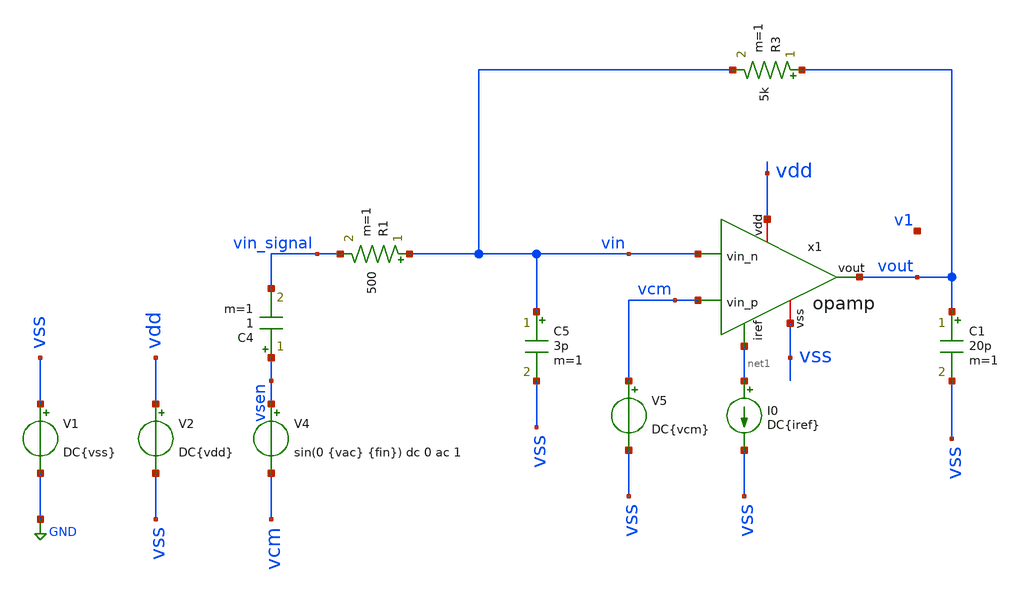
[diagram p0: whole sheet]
** sch_path: opamp/fftb_opamp_closeloop.sch
**.subckt fftb_opamp_closeloop
V1 vss GND DC{vss}
V2 vdd vss DC{vdd}
V4 vsen vcm sin(0 {vac} {fin}) dc 0 ac 1
C4 vsen vin_signal 1 m=1
I0 net1 vss DC{iref}
R1 vin vin_signal 500 m=1
R3 vout vin 5k m=1
C5 vin vss 3p m=1
C1 vout vss 20p m=1
V5 vcm vss DC{vcm}
x1 vdd net1 vin vcm vout vss v1 opamp
**** begin user architecture code




* Circuit Parameters
.param iref = 105u
.param vdd  = 1.98
.param vss  = 0.0
.param vcm  = 0.88
.param vac  = 60m
.param fin  = 9.765625e5
.options TEMP = 0

* FFT Parameters
.param Ts_FFT     = 1e-9
.csparam Ts_FFT   = {Ts_FFT}
.param fin_approx = 1e6
.param NFFT       = 4096
.csparam NFFT     = {NFFT}
.param vac_fin    = 'floor(fin_approx*Ts_FFT*NFFT)/Ts_FFT/NFFT'
.csparam Ti_FFT   = 3u
.csparam vac_fin  = {vac_fin}

* Include Models
*.lib ~/skywater/skywater-pdk/libraries/sky130_fd_pr_ngspice/latest/models/corners/sky130.lib TT
*.lib /foss/pdks/sky130A/libs.tech/ngspice/sky130.lib.spice.tt.red tt
*.lib ~/skywater/skywater-pdk/libraries/sky130_fd_pr_ngspice/latest/models/corners/sky130.lib TT
.lib /foss/pdks/sky130A/libs.tech/ngspice/sky130.lib.spice ff
*.lib /foss/pdks/sky130A/libs.tech/ngspice/sky130.lib.spice.tt.red tt
* OP Parameters & Singals to save
.save all  @M.X1.XM1.msky130_fd_pr__pfet_01v8_lvt[id] @M.X1.XM1.msky130_fd_pr__pfet_01v8_lvt[vth] @M.X1.XM1.msky130_fd_pr__pfet_01v8_lvt[vgs] @M.X1.XM1.msky130_fd_pr__pfet_01v8_lvt[vds] @M.X1.XM1.msky130_fd_pr__pfet_01v8_lvt[vdsat] @M.X1.XM1.msky130_fd_pr__pfet_01v8_lvt[gm] @M.X1.XM1.msky130_fd_pr__pfet_01v8_lvt[gds]  @M.X1.XM2.msky130_fd_pr__pfet_01v8_lvt[id] @M.X1.XM2.msky130_fd_pr__pfet_01v8_lvt[vth] @M.X1.XM2.msky130_fd_pr__pfet_01v8_lvt[vgs] @M.X1.XM2.msky130_fd_pr__pfet_01v8_lvt[vds] @M.X1.XM2.msky130_fd_pr__pfet_01v8_lvt[vdsat] @M.X1.XM2.msky130_fd_pr__pfet_01v8_lvt[gm] @M.X1.XM2.msky130_fd_pr__pfet_01v8_lvt[gds]  @M.X1.XM3.msky130_fd_pr__nfet_01v8[id] @M.X1.XM3.msky130_fd_pr__nfet_01v8[vth] @M.X1.XM3.msky130_fd_pr__nfet_01v8[vgs] @M.X1.XM3.msky130_fd_pr__nfet_01v8[vds] @M.X1.XM3.msky130_fd_pr__nfet_01v8[vdsat] @M.X1.XM3.msky130_fd_pr__nfet_01v8[gm] @M.X1.XM3.msky130_fd_pr__nfet_01v8[gds]  @M.X1.XM4.msky130_fd_pr__nfet_01v8[id] @M.X1.XM4.msky130_fd_pr__nfet_01v8[vth] @M.X1.XM4.msky130_fd_pr__nfet_01v8[vgs] @M.X1.XM4.msky130_fd_pr__nfet_01v8[vds] @M.X1.XM4.msky130_fd_pr__nfet_01v8[vdsat] @M.X1.XM4.msky130_fd_pr__nfet_01v8[gm] @M.X1.XM4.msky130_fd_pr__nfet_01v8[gds]  @M.X1.XM5.msky130_fd_pr__pfet_01v8[id] @M.X1.XM5.msky130_fd_pr__pfet_01v8[vth] @M.X1.XM5.msky130_fd_pr__pfet_01v8[vgs] @M.X1.XM5.msky130_fd_pr__pfet_01v8[vds] @M.X1.XM5.msky130_fd_pr__pfet_01v8[vdsat] @M.X1.XM5.msky130_fd_pr__pfet_01v8[gm] @M.X1.XM5.msky130_fd_pr__pfet_01v8[gds]  @M.X1.XM6.msky130_fd_pr__nfet_01v8[id] @M.X1.XM6.msky130_fd_pr__nfet_01v8[vth] @M.X1.XM6.msky130_fd_pr__nfet_01v8[vgs] @M.X1.XM6.msky130_fd_pr__nfet_01v8[vds] @M.X1.XM6.msky130_fd_pr__nfet_01v8[vdsat] @M.X1.XM6.msky130_fd_pr__nfet_01v8[gm] @M.X1.XM6.msky130_fd_pr__nfet_01v8[gds]  @M.X1.XM7.msky130_fd_pr__pfet_01v8[id] @M.X1.XM7.msky130_fd_pr__pfet_01v8[vth] @M.X1.XM7.msky130_fd_pr__pfet_01v8[vgs] @M.X1.XM7.msky130_fd_pr__pfet_01v8[vds] @M.X1.XM7.msky130_fd_pr__pfet_01v8[vdsat] @M.X1.XM7.msky130_fd_pr__pfet_01v8[gm] @M.X1.XM7.msky130_fd_pr__pfet_01v8[gds]  @M.X1.XM8.msky130_fd_pr__pfet_01v8[id] @M.X1.XM8.msky130_fd_pr__pfet_01v8[vth] @M.X1.XM8.msky130_fd_pr__pfet_01v8[vgs] @M.X1.XM8.msky130_fd_pr__pfet_01v8[vds] @M.X1.XM8.msky130_fd_pr__pfet_01v8[vdsat] @M.X1.XM8.msky130_fd_pr__pfet_01v8[gm] @M.X1.XM8.msky130_fd_pr__pfet_01v8[gds]  @M.X1.XM9.msky130_fd_pr__nfet_01v8[id] @M.X1.XM9.msky130_fd_pr__nfet_01v8[vth] @M.X1.XM9.msky130_fd_pr__nfet_01v8[vgs] @M.X1.XM9.msky130_fd_pr__nfet_01v8[vds] @M.X1.XM9.msky130_fd_pr__nfet_01v8[vdsat] @M.X1.XM9.msky130_fd_pr__nfet_01v8[gm] @M.X1.XM9.msky130_fd_pr__nfet_01v8[gds]

*Simulation
.control
  set color0 = white

  ac dec 100 1k 10G
  setplot ac1
  meas ac GBW when vdb(vout)=0
  meas ac DCG find vdb(vout) at=1k
  meas ac PM find vp(vout) when vdb(vout)=0
  print PM*180/PI
  plot vdb(vout) {vp(vout)*180/PI} vdb(v1) {vp(v1)*180/PI}

  reset
  tran 0.01u 11u
  setplot tran1
  plot v(vsen) v(vout)

  *reset
  *set sqrnoise
  *noise v(vout) V4 dec 100 1k 10G 1
  *let onoise_total_integrado = maximum(sqrt(integ(onoise_spectrum)))
  *print onoise_total_integrado



  reset
  tran 0.001u 11u
  fourier 9.765625e5 vout
  let THD_db = db(fourier11[1][3]/fourier11[1][1])
  print THD_db
  let lin-tstart = {Ti_FFT} $ skip the start - up phase
  let lin-tstep = {Ts_FFT}
  let lin-tstop = {Ti_FFT + (NFFT-1) * Ts_FFT} $ end earlier
  linearize vout
  set specwindow = none
 fft vout
  plot mag(vout)
  plot db(mag(vout)) xlimit 0 20e6

  reset
  op
  setplot op1
  unset filetype
  write tb_opamp_closeloop.raw


  reset
  noise v(vout) V4 dec 100 1k 10G 1
  setplot noise1
  plot onoise_spectrum
  setplot noise2
  print inoise_total
  print onoise_total
  print onoise_total.m.x1.xm1.msky130_fd_pr__pfet_01v8_lvt.1overf
  print onoise_total.m.x1.xm1.msky130_fd_pr__pfet_01v8_lvt.id
  print onoise_total.m.x1.xm2.msky130_fd_pr__pfet_01v8_lvt.1overf
  print onoise_total.m.x1.xm2.msky130_fd_pr__pfet_01v8_lvt.id
  print onoise_total.m.x1.xm3.msky130_fd_pr__nfet_01v8.1overf
  print onoise_total.m.x1.xm3.msky130_fd_pr__nfet_01v8.id
  print onoise_total.m.x1.xm4.msky130_fd_pr__nfet_01v8.1overf
  print onoise_total.m.x1.xm4.msky130_fd_pr__nfet_01v8.id
  print onoise_total.m.x1.xm5.msky130_fd_pr__pfet_01v8.1overf
  print onoise_total.m.x1.xm5.msky130_fd_pr__pfet_01v8.id
  print onoise_total.m.x1.xm6.msky130_fd_pr__nfet_01v8.1overf
  print onoise_total.m.x1.xm6.msky130_fd_pr__nfet_01v8.id
  print onoise_total.m.x1.xm7.msky130_fd_pr__pfet_01v8.1overf
  print onoise_total.m.x1.xm7.msky130_fd_pr__pfet_01v8.id
  vprint onoise_total.m.x1.xm8.msky130_fd_pr__pfet_01v8.1overf
  print onoise_total.m.x1.xm8.msky130_fd_pr__pfet_01v8.id
  set filetype=ascii
  write tpfinal_noise.raw
.endc

.end


**** end user architecture code
**.ends

* expanding   symbol:  opamp.sym # of pins=7
** sym_path: opamp/opamp.sym
** sch_path: opamp/opamp.sch
.subckt opamp vdd iref vin_n vin_p vout vss v1
*.iopin vdd
*.iopin vss
*.ipin vin_n
*.ipin vin_p
*.ipin iref
*.opin vout
*.opin v1
XM5 vp iref vdd vdd sky130_fd_pr__pfet_01v8 L=0.3 W=50 nf=1 ad='W * 0.29' as='W * 0.29' pd='2 * (W + 0.29)'
+ ps='2 * (W + 0.29)' nrd='0.29 / W' nrs='0.29 / W' sa=0 sb=0 sd=0 mult=15 m=15
XM7 vout iref vdd vdd sky130_fd_pr__pfet_01v8 L=0.3 W=50 nf=1 ad='W * 0.29' as='W * 0.29' pd='2 * (W + 0.29)'
+ ps='2 * (W + 0.29)' nrd='0.29 / W' nrs='0.29 / W' sa=0 sb=0 sd=0 mult=24 m=24
XM8 iref iref vdd vdd sky130_fd_pr__pfet_01v8 L=0.3 W=50 nf=1 ad='W * 0.29' as='W * 0.29' pd='2 * (W + 0.29)'
+ ps='2 * (W + 0.29)' nrd='0.29 / W' nrs='0.29 / W' sa=0 sb=0 sd=0 mult=3 m=3
XM1 vbn vin_n vp vp sky130_fd_pr__pfet_01v8_lvt L=0.6 W=86 nf=1 ad='int((nf+1)/2) * W/nf * 0.29' as='int((nf+2)/2) * W/nf * 0.29'
+ pd='2*int((nf+1)/2) * (W/nf + 0.29)' ps='2*int((nf+2)/2) * (W/nf + 0.29)' nrd='0.29 / W' nrs='0.29 / W'
+ sa=0 sb=0 sd=0 mult=10 m=10
XM2 v1 vin_p vp vp sky130_fd_pr__pfet_01v8_lvt L=0.6 W=86 nf=1 ad='int((nf+1)/2) * W/nf * 0.29' as='int((nf+2)/2) * W/nf * 0.29'
+ pd='2*int((nf+1)/2) * (W/nf + 0.29)' ps='2*int((nf+2)/2) * (W/nf + 0.29)' nrd='0.29 / W' nrs='0.29 / W'
+ sa=0 sb=0 sd=0 mult=10 m=10
C1 net2 vout 5.77p m=1
Vmeas net1 vss 0
.save i(vmeas)
XM6 vout v1 net1 net1 sky130_fd_pr__nfet_01v8 L=0.3 W=44 nf=1 ad='W * 0.29' as='W * 0.29' pd='2 * (W + 0.29)'
+ ps='2 * (W + 0.29)' nrd='0.29 / W' nrs='0.29 / W' sa=0 sb=0 sd=0 mult=9 m=9
XM4 v1 vbn net1 net1 sky130_fd_pr__nfet_01v8 L=2.3 W=30 nf=1 ad='W * 0.29' as='W * 0.29' pd='2 * (W + 0.29)'
+ ps='2 * (W + 0.29)' nrd='0.29 / W' nrs='0.29 / W' sa=0 sb=0 sd=0 mult=2 m=2
XM3 vbn vbn net1 net1 sky130_fd_pr__nfet_01v8 L=2.3 W=30 nf=1 ad='W * 0.29' as='W * 0.29' pd='2 * (W + 0.29)'
+ ps='2 * (W + 0.29)' nrd='0.29 / W' nrs='0.29 / W' sa=0 sb=0 sd=0 mult=2 m=2
XM9 net2 vdd v1 vss sky130_fd_pr__nfet_01v8 L=0.38 W=12 nf=1 ad='W * 0.29' as='W * 0.29' pd='2 * (W + 0.29)'
+ ps='2 * (W + 0.29)' nrd='0.29 / W' nrs='0.29 / W' sa=0 sb=0 sd=0 mult=1 m=1
.ends

.GLOBAL GND
.end
